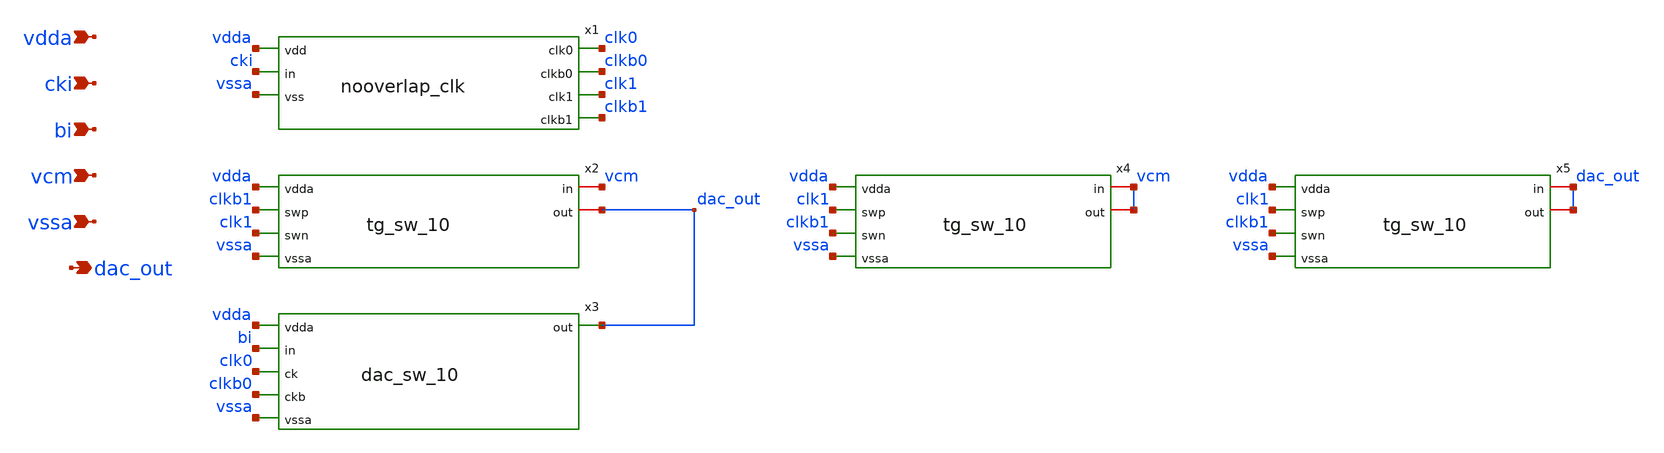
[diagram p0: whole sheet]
** sch_path: xschem/cdac_sw_10.sch
**.subckt cdac_sw_10 vdda cki bi vcm vssa dac_out
*.ipin vdda
*.ipin cki
*.ipin bi
*.ipin vcm
*.ipin vssa
*.opin dac_out
x1 vdda cki vssa clk0 clkb0 clk1 clkb1 nooverlap_clk
x2 vdda clkb1 clk1 vssa vcm dac_out tg_sw_10
x3 vdda bi clk0 clkb0 vssa dac_out dac_sw_10
x4 vdda clk1 clkb1 vssa vcm vcm tg_sw_10
x5 vdda clk1 clkb1 vssa dac_out dac_out tg_sw_10
**.ends

* expanding   symbol:  nooverlap_clk.sym # of pins=7
** sym_path: xschem/nooverlap_clk.sym
** sch_path: xschem/nooverlap_clk.sch
.subckt nooverlap_clk vdd in vss clk0 clkb0 clk1 clkb1
*.ipin vdd
*.ipin in
*.ipin vss
*.opin clk0
*.opin clkb0
*.opin clk1
*.opin clkb1
x1 in a vss vss vdd vdd net5 sky130_fd_sc_hd__nand2_1
x2 b net1 vss vss vdd vdd net2 sky130_fd_sc_hd__nand2_1
x3 in vss vss vdd vdd net1 sky130_fd_sc_hd__inv_1
x4 net5 vss vss vdd vdd net4 sky130_fd_sc_hd__inv_1
x5 net2 vss vss vdd vdd net3 sky130_fd_sc_hd__inv_1
x6 net4 vss vss vdd vdd b sky130_fd_sc_hd__inv_1
x7 net3 vss vss vdd vdd a sky130_fd_sc_hd__inv_1
x8 b vss vss vdd vdd net6 sky130_fd_sc_hd__inv_4
x9 a vss vss vdd vdd net7 sky130_fd_sc_hd__inv_4
x10 net6 vss vss vdd vdd clkb0 sky130_fd_sc_hd__inv_8
x11 net7 vss vss vdd vdd clkb1 sky130_fd_sc_hd__inv_8
x12 clkb0 vss vss vdd vdd clk0 sky130_fd_sc_hd__inv_8
x13 clkb1 vss vss vdd vdd clk1 sky130_fd_sc_hd__inv_8
**** begin user architecture code

.include /usr/local/share/pdk/sky130A/libs.ref/sky130_fd_sc_hd/spice/sky130_fd_sc_hd.spice

**** end user architecture code
.ends


* expanding   symbol:  tg_sw_10.sym # of pins=6
** sym_path: xschem/tg_sw_10.sym
** sch_path: xschem/tg_sw_10.sch
.subckt tg_sw_10 vdda swp swn vssa in out
*.ipin vdda
*.ipin swp
*.ipin swn
*.ipin vssa
*.iopin in
*.iopin out
XM1 in swp out vdda sky130_fd_pr__pfet_01v8 L=0.5 W=1.5 nf=1 ad='int((nf+1)/2) * W/nf * 0.29' as='int((nf+2)/2) * W/nf * 0.29'
+ pd='2*int((nf+1)/2) * (W/nf + 0.29)' ps='2*int((nf+2)/2) * (W/nf + 0.29)' nrd='0.29 / W' nrs='0.29 / W'
+ sa=0 sb=0 sd=0 mult=2 m=2
XM2 in swn out vssa sky130_fd_pr__nfet_01v8 L=0.5 W=0.5 nf=1 ad='int((nf+1)/2) * W/nf * 0.29' as='int((nf+2)/2) * W/nf * 0.29'
+ pd='2*int((nf+1)/2) * (W/nf + 0.29)' ps='2*int((nf+2)/2) * (W/nf + 0.29)' nrd='0.29 / W' nrs='0.29 / W'
+ sa=0 sb=0 sd=0 mult=2 m=2
.ends


* expanding   symbol:  dac_sw_10.sym # of pins=6
** sym_path: xschem/dac_sw_10.sym
** sch_path: xschem/dac_sw_10.sch
.subckt dac_sw_10 vdda in ck ckb vssa out
*.ipin vdda
*.ipin in
*.ipin ck
*.ipin ckb
*.ipin vssa
*.opin out
XM1 net1 in vdda vdda sky130_fd_pr__pfet_01v8 L=0.5 W=1.5 nf=1 ad='int((nf+1)/2) * W/nf * 0.29' as='int((nf+2)/2) * W/nf * 0.29'
+ pd='2*int((nf+1)/2) * (W/nf + 0.29)' ps='2*int((nf+2)/2) * (W/nf + 0.29)' nrd='0.29 / W' nrs='0.29 / W'
+ sa=0 sb=0 sd=0 mult=2 m=2
XM2 out ckb net1 vdda sky130_fd_pr__pfet_01v8 L=0.5 W=1.5 nf=1 ad='int((nf+1)/2) * W/nf * 0.29' as='int((nf+2)/2) * W/nf * 0.29'
+ pd='2*int((nf+1)/2) * (W/nf + 0.29)' ps='2*int((nf+2)/2) * (W/nf + 0.29)' nrd='0.29 / W' nrs='0.29 / W'
+ sa=0 sb=0 sd=0 mult=2 m=2
XM3 out ck net2 vssa sky130_fd_pr__nfet_01v8 L=0.5 W=0.5 nf=1 ad='int((nf+1)/2) * W/nf * 0.29' as='int((nf+2)/2) * W/nf * 0.29'
+ pd='2*int((nf+1)/2) * (W/nf + 0.29)' ps='2*int((nf+2)/2) * (W/nf + 0.29)' nrd='0.29 / W' nrs='0.29 / W'
+ sa=0 sb=0 sd=0 mult=2 m=2
XM4 net2 in vssa vssa sky130_fd_pr__nfet_01v8 L=0.5 W=0.5 nf=1 ad='int((nf+1)/2) * W/nf * 0.29' as='int((nf+2)/2) * W/nf * 0.29'
+ pd='2*int((nf+1)/2) * (W/nf + 0.29)' ps='2*int((nf+2)/2) * (W/nf + 0.29)' nrd='0.29 / W' nrs='0.29 / W'
+ sa=0 sb=0 sd=0 mult=2 m=2
.ends

.end
